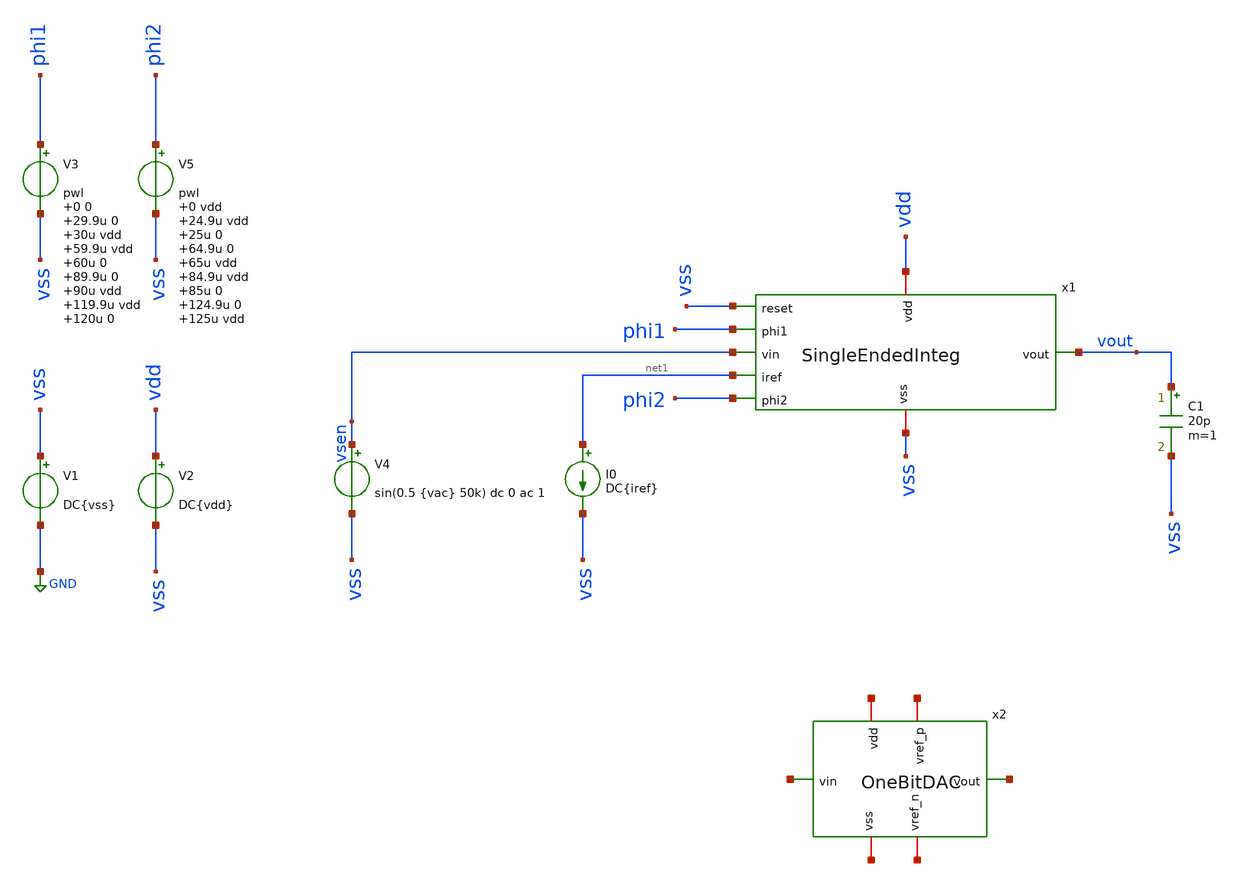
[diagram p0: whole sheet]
** sch_path: xschem/SigmaDelta_tb.sch
**.subckt SigmaDelta_tb
x1 vss phi1 vdd vsen vout net1 phi2 vss SingleEndedInteg
V1 vss GND DC{vss}
V2 vdd vss DC{vdd}
I0 net1 vss DC{iref}
C1 vout vss 20p m=1
V4 vsen vss sin(0.5 {vac} 50k) dc 0 ac 1
V3 phi1 vss pwl 0 0 29.9u 0 30u vdd 59.9u vdd 60u 0 89.9u 0 90u vdd 119.9u vdd 120u 0
V5 phi2 vss pwl 0 vdd 24.9u vdd 25u 0 64.9u 0 65u vdd 84.9u vdd 85u 0 124.9u 0 125u vdd
x2 net2 net3 net4 net5 net6 net7 OneBitDAC
**** begin user architecture code




* Circuit Parameters
.param iref = 100u
.param vdd  = 1.8
.param vss  = 0.0
.param vcm  = 0.8
.param vac  = 0.5
.options TEMP = 65.0

* Include Models
.lib /home/filippo/work/PDKs/sky130A/libs.tech/ngspice/sky130.lib.spice tt

* OP Parameters & Singals to save
.save all
*+ @M.X1.XM1.msky130_fd_pr__pfet_01v8[id] @M.X1.XM1.msky130_fd_pr__pfet_01v8[vth]
*+ @M.X1.XM1.msky130_fd_pr__pfet_01v8[vgs] @M.X1.XM1.msky130_fd_pr__pfet_01v8[vds] @M.X1.XM1.msky130_fd_pr__pfet_01v8[vdsat]
*+ @M.X1.XM1.msky130_fd_pr__pfet_01v8[gm] @M.X1.XM1.msky130_fd_pr__pfet_01v8[gds]
*+ @M.X1.XM2.msky130_fd_pr__pfet_01v8[id] @M.X1.XM2.msky130_fd_pr__pfet_01v8[vth]
*+ @M.X1.XM2.msky130_fd_pr__pfet_01v8[vgs] @M.X1.XM2.msky130_fd_pr__pfet_01v8[vds] @M.X1.XM2.msky130_fd_pr__pfet_01v8[vdsat]
*+ @M.X1.XM2.msky130_fd_pr__pfet_01v8[gm] @M.X1.XM2.msky130_fd_pr__pfet_01v8[gds]
*+ @M.X1.XM3.msky130_fd_pr__nfet_01v8[id] @M.X1.XM3.msky130_fd_pr__nfet_01v8[vth]
*+ @M.X1.XM3.msky130_fd_pr__nfet_01v8[vgs] @M.X1.XM3.msky130_fd_pr__nfet_01v8[vds] @M.X1.XM3.msky130_fd_pr__nfet_01v8[vdsat]
*+ @M.X1.XM3.msky130_fd_pr__nfet_01v8[gm] @M.X1.XM3.msky130_fd_pr__nfet_01v8[gds]
*+ @M.X1.XM4.msky130_fd_pr__nfet_01v8[id] @M.X1.XM4.msky130_fd_pr__nfet_01v8[vth]
*+ @M.X1.XM4.msky130_fd_pr__nfet_01v8[vgs] @M.X1.XM4.msky130_fd_pr__nfet_01v8[vds] @M.X1.XM4.msky130_fd_pr__nfet_01v8[vdsat]
*+ @M.X1.XM4.msky130_fd_pr__nfet_01v8[gm] @M.X1.XM4.msky130_fd_pr__nfet_01v8[gds]
*+ @M.X1.XM5.msky130_fd_pr__pfet_01v8[id] @M.X1.XM5.msky130_fd_pr__pfet_01v8[vth]
*+ @M.X1.XM5.msky130_fd_pr__pfet_01v8[vgs] @M.X1.XM5.msky130_fd_pr__pfet_01v8[vds] @M.X1.XM5.msky130_fd_pr__pfet_01v8[vdsat]
*+ @M.X1.XM5.msky130_fd_pr__pfet_01v8[gm] @M.X1.XM5.msky130_fd_pr__pfet_01v8[gds]
*+ @M.X1.XM6.msky130_fd_pr__nfet_01v8[id] @M.X1.XM6.msky130_fd_pr__nfet_01v8[vth]
*+ @M.X1.XM6.msky130_fd_pr__nfet_01v8[vgs] @M.X1.XM6.msky130_fd_pr__nfet_01v8[vds] @M.X1.XM6.msky130_fd_pr__nfet_01v8[vdsat]
*+ @M.X1.XM6.msky130_fd_pr__nfet_01v8[gm] @M.X1.XM6.msky130_fd_pr__nfet_01v8[gds]
*+ @M.X1.XM7.msky130_fd_pr__pfet_01v8[id] @M.X1.XM7.msky130_fd_pr__pfet_01v8[vth]
*+ @M.X1.XM7.msky130_fd_pr__pfet_01v8[vgs] @M.X1.XM7.msky130_fd_pr__pfet_01v8[vds] @M.X1.XM7.msky130_fd_pr__pfet_01v8[vdsat]
*+ @M.X1.XM7.msky130_fd_pr__pfet_01v8[gm] @M.X1.XM7.msky130_fd_pr__pfet_01v8[gds]
*+ @M.X1.XM8.msky130_fd_pr__pfet_01v8[id] @M.X1.XM8.msky130_fd_pr__pfet_01v8[vth]
*+ @M.X1.XM8.msky130_fd_pr__pfet_01v8[vgs] @M.X1.XM8.msky130_fd_pr__pfet_01v8[vds] @M.X1.XM8.msky130_fd_pr__pfet_01v8[vdsat]
*+ @M.X1.XM8.msky130_fd_pr__pfet_01v8[gm] @M.X1.XM8.msky130_fd_pr__pfet_01v8[gds]
*+ @M.X1.XM9.msky130_fd_pr__nfet_01v8[id] @M.X1.XM9.msky130_fd_pr__nfet_01v8[vth]
*+ @M.X1.XM9.msky130_fd_pr__nfet_01v8[vgs] @M.X1.XM9.msky130_fd_pr__nfet_01v8[vds] @M.X1.XM9.msky130_fd_pr__nfet_01v8[vdsat]
*+ @M.X1.XM9.msky130_fd_pr__nfet_01v8[gm] @M.X1.XM9.msky130_fd_pr__nfet_01v8[gds]

*Simulations
.control
  tran 0.01u 150u
  setplot tran1
  plot v(vsen) v(vout) v(phi1) v(phi2)
  write /foss/designs/SigmaDelta_ADC/xschem/sim_results/OpAmpinteg.raw

.endc

.end


**** end user architecture code
**.ends

* expanding   symbol:  SingleEndedInteg.sym # of pins=8
** sym_path: xschem/SingleEndedInteg.sym
** sch_path: xschem/SingleEndedInteg.sch
.subckt SingleEndedInteg reset phi1 vdd vin vout iref phi2 vss
*.iopin vss
*.ipin vin
*.ipin iref
*.iopin vdd
*.opin vout
*.ipin phi1
*.ipin phi2
*.ipin reset
XC1 net2 net1 sky130_fd_pr__cap_mim_m3_1 W=17.55 L=15 MF=6 m=6
XM12 net3 phi2 net1 vss sky130_fd_pr__nfet_01v8 L=0.15 W=0.75 nf=1 ad='W * 0.29' as='W * 0.29' pd='2 * (W + 0.29)'
+ ps='2 * (W + 0.29)' nrd='0.29 / W' nrs='0.29 / W' sa=0 sb=0 sd=0 mult=6 m=6
XM13 net1 phi1 vss vss sky130_fd_pr__nfet_01v8 L=0.15 W=0.75 nf=1 ad='W * 0.29' as='W * 0.29' pd='2 * (W + 0.29)'
+ ps='2 * (W + 0.29)' nrd='0.29 / W' nrs='0.29 / W' sa=0 sb=0 sd=0 mult=6 m=6
XM10 net2 phi1 vin vss sky130_fd_pr__nfet_01v8 L=0.15 W=0.75 nf=1 ad='W * 0.29' as='W * 0.29' pd='2 * (W + 0.29)'
+ ps='2 * (W + 0.29)' nrd='0.29 / W' nrs='0.29 / W' sa=0 sb=0 sd=0 mult=6 m=6
XM11 vss phi2 net2 vss sky130_fd_pr__nfet_01v8 L=0.15 W=0.75 nf=1 ad='W * 0.29' as='W * 0.29' pd='2 * (W + 0.29)'
+ ps='2 * (W + 0.29)' nrd='0.29 / W' nrs='0.29 / W' sa=0 sb=0 sd=0 mult=6 m=6
XC2 net3 vout sky130_fd_pr__cap_mim_m3_1 W=17.55 L=15 MF=6 m=6
XM14 net3 reset vout vss sky130_fd_pr__nfet_01v8 L=0.15 W=0.75 nf=1 ad='W * 0.29' as='W * 0.29' pd='2 * (W + 0.29)'
+ ps='2 * (W + 0.29)' nrd='0.29 / W' nrs='0.29 / W' sa=0 sb=0 sd=0 mult=6 m=6
x1 net3 net4 net5 vss vss net6 OpAmp
.ends


* expanding   symbol:  OneBitDAC.sym # of pins=6
** sym_path: xschem/OneBitDAC.sym
** sch_path: xschem/OneBitDAC.sch
.subckt OneBitDAC vref_p vdd vin vout vref_n vss
*.iopin vdd
*.iopin vss
*.ipin vin
*.iopin vref_p
*.iopin vref_n
*.opin vout
XM8 net1 vin vdd vdd sky130_fd_pr__pfet_01v8 L=0.6 W=6 nf=1 ad='W * 0.29' as='W * 0.29' pd='2 * (W + 0.29)'
+ ps='2 * (W + 0.29)' nrd='0.29 / W' nrs='0.29 / W' sa=0 sb=0 sd=0 mult=1 m=1
XM1 net1 vin vss vss sky130_fd_pr__nfet_01v8 L=0.6 W=3 nf=1 ad='int((nf+1)/2) * W/nf * 0.29' as='int((nf+2)/2) * W/nf * 0.29'
+ pd='2*int((nf+1)/2) * (W/nf + 0.29)' ps='2*int((nf+2)/2) * (W/nf + 0.29)' nrd='0.29 / W' nrs='0.29 / W'
+ sa=0 sb=0 sd=0 mult=1 m=1
XM2 vout net1 vref_p vdd sky130_fd_pr__pfet_01v8 L=0.6 W=8.2 nf=1 ad='int((nf+1)/2) * W/nf * 0.29' as='int((nf+2)/2) * W/nf * 0.29'
+ pd='2*int((nf+1)/2) * (W/nf + 0.29)' ps='2*int((nf+2)/2) * (W/nf + 0.29)' nrd='0.29 / W' nrs='0.29 / W'
+ sa=0 sb=0 sd=0 mult=1 m=1
XM3 vout net1 vref_n vss sky130_fd_pr__nfet_01v8 L=0.6 W=4.2 nf=1 ad='int((nf+1)/2) * W/nf * 0.29' as='int((nf+2)/2) * W/nf * 0.29'
+ pd='2*int((nf+1)/2) * (W/nf + 0.29)' ps='2*int((nf+2)/2) * (W/nf + 0.29)' nrd='0.29 / W' nrs='0.29 / W'
+ sa=0 sb=0 sd=0 mult=1 m=1
XM4 vref_p vin vout vss sky130_fd_pr__nfet_01v8 L=0.6 W=4.2 nf=1 ad='int((nf+1)/2) * W/nf * 0.29' as='int((nf+2)/2) * W/nf * 0.29'
+ pd='2*int((nf+1)/2) * (W/nf + 0.29)' ps='2*int((nf+2)/2) * (W/nf + 0.29)' nrd='0.29 / W' nrs='0.29 / W'
+ sa=0 sb=0 sd=0 mult=1 m=1
XM5 vref_n vin vout vdd sky130_fd_pr__pfet_01v8 L=0.6 W=8.2 nf=1 ad='int((nf+1)/2) * W/nf * 0.29' as='int((nf+2)/2) * W/nf * 0.29'
+ pd='2*int((nf+1)/2) * (W/nf + 0.29)' ps='2*int((nf+2)/2) * (W/nf + 0.29)' nrd='0.29 / W' nrs='0.29 / W'
+ sa=0 sb=0 sd=0 mult=1 m=1
.ends

.GLOBAL GND
.end
